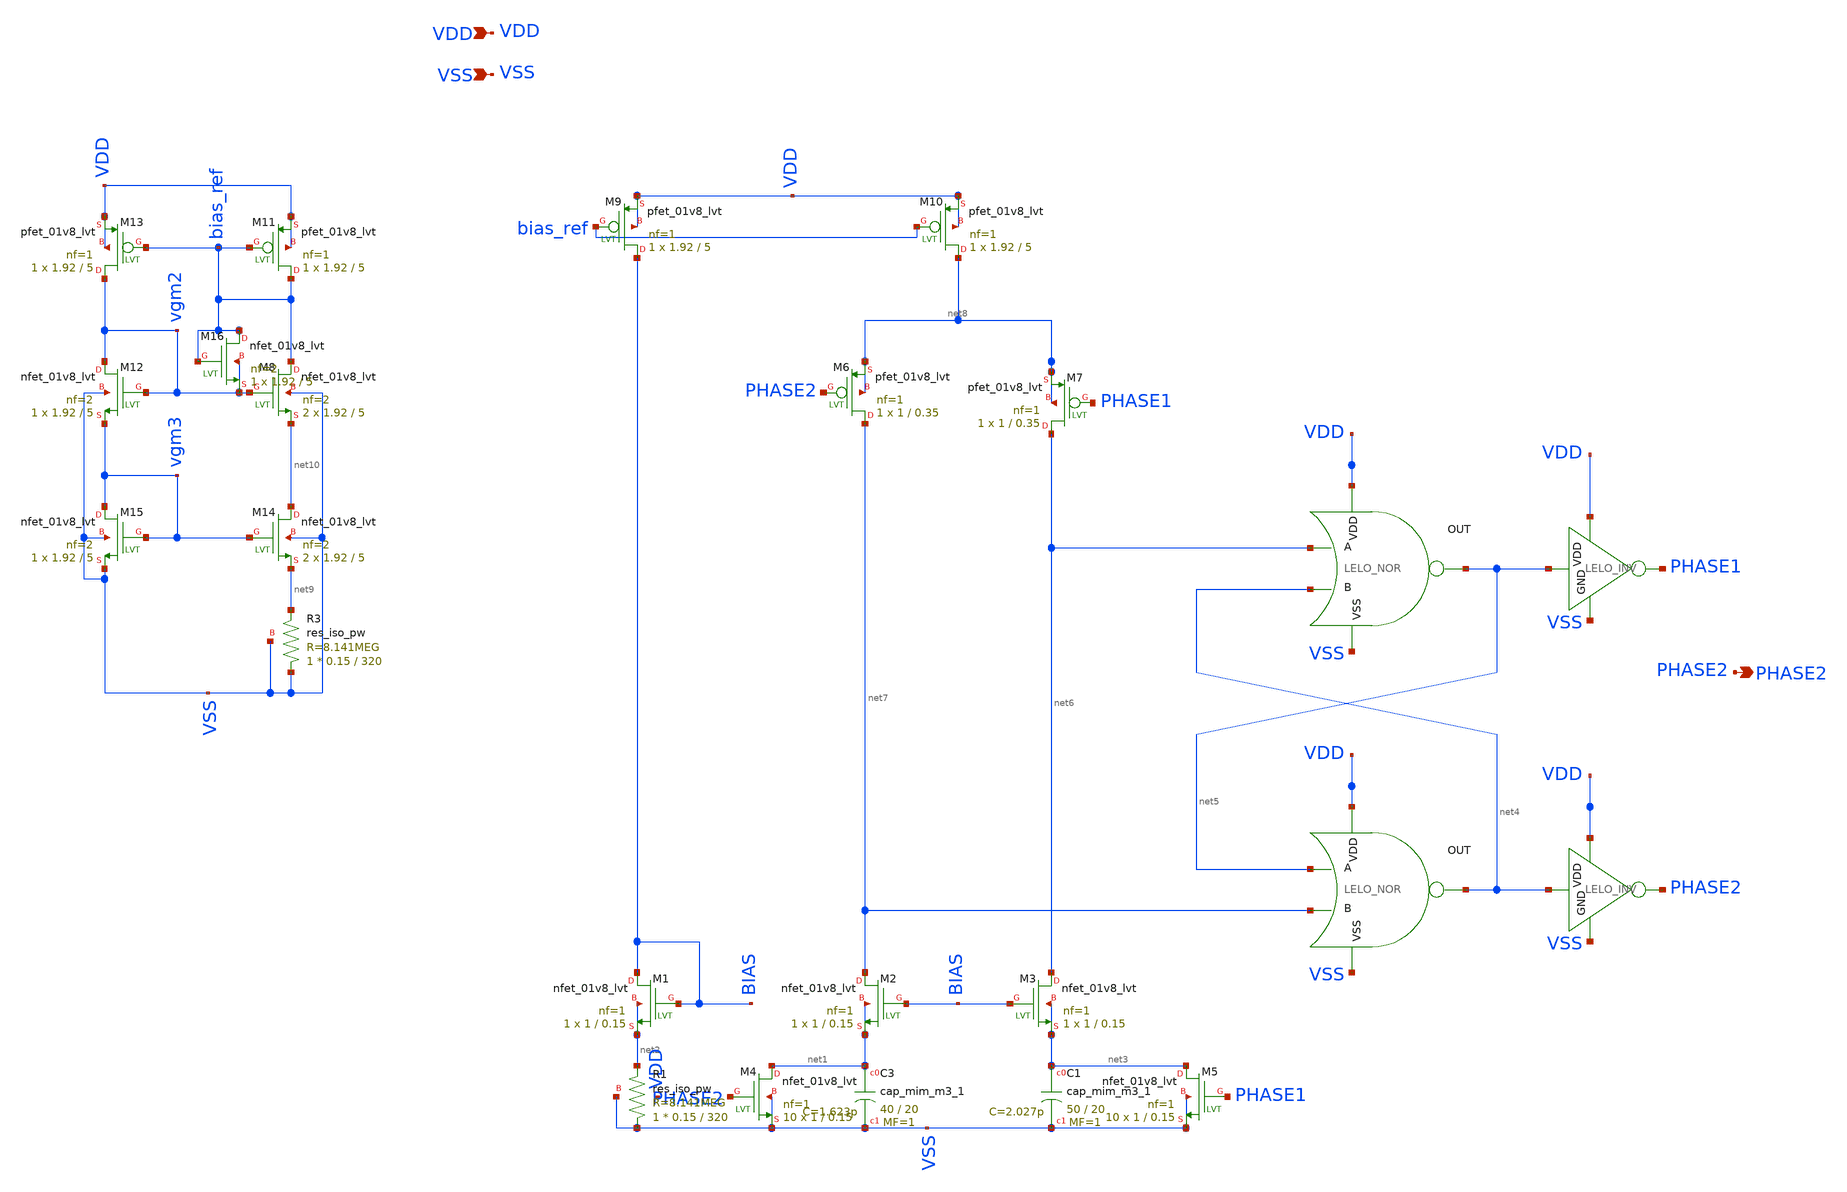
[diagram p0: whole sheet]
** sch_path: design/LELO_SVOD_SKY130A/LELO_SVOD_RELOSC.sch
**.subckt LELO_SVOD_RELOSC VDD VSS PHASE2
*.ipin VDD
*.ipin VSS
*.opin PHASE2
XM1 BIAS BIAS net2 net2 sky130_fd_pr__nfet_01v8_lvt L=0.15 W=1 nf=1 ad='int((1 + 1)/2) * 1 / 1 * 0.29'
+ as='int((1 + 2)/2) * 1 / 1 * 0.29' pd='2*int((1 + 1)/2) * (1 / 1 + 0.29)' ps='2*int((1 + 2)/2) * (1 / 1 + 0.29)'
+ nrd='0.29 / 1 ' nrs='0.29 / 1 ' sa=0 sb=0 sd=0 mult=1 m=1
XM2 net7 BIAS net1 net1 sky130_fd_pr__nfet_01v8_lvt L=0.15 W=1 nf=1 ad='int((1 + 1)/2) * 1 / 1 * 0.29'
+ as='int((1 + 2)/2) * 1 / 1 * 0.29' pd='2*int((1 + 1)/2) * (1 / 1 + 0.29)' ps='2*int((1 + 2)/2) * (1 / 1 + 0.29)'
+ nrd='0.29 / 1 ' nrs='0.29 / 1 ' sa=0 sb=0 sd=0 mult=1 m=1
XM3 net6 BIAS net3 net3 sky130_fd_pr__nfet_01v8_lvt L=0.15 W=1 nf=1 ad='int((1 + 1)/2) * 1 / 1 * 0.29'
+ as='int((1 + 2)/2) * 1 / 1 * 0.29' pd='2*int((1 + 1)/2) * (1 / 1 + 0.29)' ps='2*int((1 + 2)/2) * (1 / 1 + 0.29)'
+ nrd='0.29 / 1 ' nrs='0.29 / 1 ' sa=0 sb=0 sd=0 mult=1 m=1
XM4 net1 PHASE2 VSS VSS sky130_fd_pr__nfet_01v8_lvt L=0.15 W=1 nf=1 ad='int((1 + 1)/2) * 1 / 1 * 0.29'
+ as='int((1 + 2)/2) * 1 / 1 * 0.29' pd='2*int((1 + 1)/2) * (1 / 1 + 0.29)' ps='2*int((1 + 2)/2) * (1 / 1 + 0.29)'
+ nrd='0.29 / 1 ' nrs='0.29 / 1 ' sa=0 sb=0 sd=0 mult=10 m=10
XM5 net3 PHASE1 VSS VSS sky130_fd_pr__nfet_01v8_lvt L=0.15 W=1 nf=1 ad='int((1 + 1)/2) * 1 / 1 * 0.29'
+ as='int((1 + 2)/2) * 1 / 1 * 0.29' pd='2*int((1 + 1)/2) * (1 / 1 + 0.29)' ps='2*int((1 + 2)/2) * (1 / 1 + 0.29)'
+ nrd='0.29 / 1 ' nrs='0.29 / 1 ' sa=0 sb=0 sd=0 mult=10 m=10
x1 VDD net5 net6 net4 VSS LELO_NOR
x2 VDD net4 net5 net7 VSS LELO_NOR
XM6 net7 PHASE2 net8 net8 sky130_fd_pr__pfet_01v8_lvt L=0.35 W=1 nf=1 ad='int((1 + 1)/2) * 1 / 1 * 0.29'
+ as='int((1 + 2)/2) * 1 / 1 * 0.29' pd='2*int((1 + 1)/2) * (1 / 1 + 0.29)' ps='2*int((1 + 2)/2) * (1 / 1 + 0.29)'
+ nrd='0.29 / 1 ' nrs='0.29 / 1 ' sa=0 sb=0 sd=0 mult=1 m=1
XM7 net6 PHASE1 net8 net8 sky130_fd_pr__pfet_01v8_lvt L=0.35 W=1 nf=1 ad='int((1 + 1)/2) * 1 / 1 * 0.29'
+ as='int((1 + 2)/2) * 1 / 1 * 0.29' pd='2*int((1 + 1)/2) * (1 / 1 + 0.29)' ps='2*int((1 + 2)/2) * (1 / 1 + 0.29)'
+ nrd='0.29 / 1 ' nrs='0.29 / 1 ' sa=0 sb=0 sd=0 mult=1 m=1
x3 VDD net5 PHASE1 VSS LELO_INV
x4 VDD net4 PHASE2 VSS LELO_INV
XM9 BIAS bias_ref VDD VDD sky130_fd_pr__pfet_01v8_lvt L=5 W=1.92 nf=1 ad='int((1 + 1)/2) * 1.92 / 1 * 0.29'
+ as='int((1 + 2)/2) * 1.92 / 1 * 0.29' pd='2*int((1 + 1)/2) * (1.92 / 1 + 0.29)' ps='2*int((1 + 2)/2) * (1.92 / 1 + 0.29)'
+ nrd='0.29 / 1.92 ' nrs='0.29 / 1.92 ' sa=0 sb=0 sd=0 mult=1 m=1
XM10 net8 bias_ref VDD VDD sky130_fd_pr__pfet_01v8_lvt L=5 W=1.92 nf=1 ad='int((1 + 1)/2) * 1.92 / 1 * 0.29'
+ as='int((1 + 2)/2) * 1.92 / 1 * 0.29' pd='2*int((1 + 1)/2) * (1.92 / 1 + 0.29)' ps='2*int((1 + 2)/2) * (1.92 / 1 + 0.29)'
+ nrd='0.29 / 1.92 ' nrs='0.29 / 1.92 ' sa=0 sb=0 sd=0 mult=1 m=1
XM8 bias_ref vgm2 net10 VSS sky130_fd_pr__nfet_01v8_lvt L=5 W=1.92 nf=2 ad='int((2 + 1)/2) * 1.92 / 2 * 0.29'
+ as='int((2 + 2)/2) * 1.92 / 2 * 0.29' pd='2*int((2 + 1)/2) * (1.92 / 2 + 0.29)' ps='2*int((2 + 2)/2) * (1.92 / 2 + 0.29)'
+ nrd='0.29 / 1.92 ' nrs='0.29 / 1.92 ' sa=0 sb=0 sd=0 mult=2 m=2
XM11 bias_ref bias_ref VDD VDD sky130_fd_pr__pfet_01v8_lvt L=5 W=1.92 nf=1 ad='int((1 + 1)/2) * 1.92 / 1 * 0.29'
+ as='int((1 + 2)/2) * 1.92 / 1 * 0.29' pd='2*int((1 + 1)/2) * (1.92 / 1 + 0.29)' ps='2*int((1 + 2)/2) * (1.92 / 1 + 0.29)'
+ nrd='0.29 / 1.92 ' nrs='0.29 / 1.92 ' sa=0 sb=0 sd=0 mult=1 m=1
XM12 vgm2 vgm2 vgm3 VSS sky130_fd_pr__nfet_01v8_lvt L=5 W=1.92 nf=2 ad='int((2 + 1)/2) * 1.92 / 2 * 0.29'
+ as='int((2 + 2)/2) * 1.92 / 2 * 0.29' pd='2*int((2 + 1)/2) * (1.92 / 2 + 0.29)' ps='2*int((2 + 2)/2) * (1.92 / 2 + 0.29)'
+ nrd='0.29 / 1.92 ' nrs='0.29 / 1.92 ' sa=0 sb=0 sd=0 mult=1 m=1
XM13 vgm2 bias_ref VDD VDD sky130_fd_pr__pfet_01v8_lvt L=5 W=1.92 nf=1 ad='int((1 + 1)/2) * 1.92 / 1 * 0.29'
+ as='int((1 + 2)/2) * 1.92 / 1 * 0.29' pd='2*int((1 + 1)/2) * (1.92 / 1 + 0.29)' ps='2*int((1 + 2)/2) * (1.92 / 1 + 0.29)'
+ nrd='0.29 / 1.92 ' nrs='0.29 / 1.92 ' sa=0 sb=0 sd=0 mult=1 m=1
XM14 net10 vgm3 net9 VSS sky130_fd_pr__nfet_01v8_lvt L=5 W=1.92 nf=2 ad='int((2 + 1)/2) * 1.92 / 2 * 0.29'
+ as='int((2 + 2)/2) * 1.92 / 2 * 0.29' pd='2*int((2 + 1)/2) * (1.92 / 2 + 0.29)' ps='2*int((2 + 2)/2) * (1.92 / 2 + 0.29)'
+ nrd='0.29 / 1.92 ' nrs='0.29 / 1.92 ' sa=0 sb=0 sd=0 mult=2 m=2
XM15 vgm3 vgm3 VSS VSS sky130_fd_pr__nfet_01v8_lvt L=5 W=1.92 nf=2 ad='int((2 + 1)/2) * 1.92 / 2 * 0.29'
+ as='int((2 + 2)/2) * 1.92 / 2 * 0.29' pd='2*int((2 + 1)/2) * (1.92 / 2 + 0.29)' ps='2*int((2 + 2)/2) * (1.92 / 2 + 0.29)'
+ nrd='0.29 / 1.92 ' nrs='0.29 / 1.92 ' sa=0 sb=0 sd=0 mult=1 m=1
XM16 bias_ref bias_ref vgm2 vgm2 sky130_fd_pr__nfet_01v8_lvt L=5 W=1.92 nf=2 ad='int((2 + 1)/2) * 1.92 / 2 * 0.29'
+ as='int((2 + 2)/2) * 1.92 / 2 * 0.29' pd='2*int((2 + 1)/2) * (1.92 / 2 + 0.29)' ps='2*int((2 + 2)/2) * (1.92 / 2 + 0.29)'
+ nrd='0.29 / 1.92 ' nrs='0.29 / 1.92 ' sa=0 sb=0 sd=0 mult=1 m=1
XC3 net1 VSS sky130_fd_pr__cap_mim_m3_1 W=40 L=20 MF=1 m=1
XC1 net3 VSS sky130_fd_pr__cap_mim_m3_1 W=50 L=20 MF=1 m=1
XR3 VSS net9 VSS sky130_fd_pr__res_iso_pw W=0.15 L=320 m=1
XR1 VSS net2 VSS sky130_fd_pr__res_iso_pw W=0.15 L=320 m=1
**.ends

* expanding   symbol:  LELO_SVOD_SKY130A/LELO_NOR.sym # of pins=5
** sym_path: design/LELO_SVOD_SKY130A/LELO_NOR.sym
** sch_path: design/LELO_SVOD_SKY130A/LELO_NOR.sch
.subckt LELO_NOR VDD OUT A B VSS
*.ipin VDD
*.ipin VSS
*.opin OUT
*.ipin A
*.ipin B
XM2 OUT B VSS VSS sky130_fd_pr__nfet_01v8 L=0.15 W=2 nf=1 ad='int((1 + 1)/2) * 2 / 1 * 0.29' as='int((1 + 2)/2) * 2 / 1 * 0.29'
+ pd='2*int((1 + 1)/2) * (2 / 1 + 0.29)' ps='2*int((1 + 2)/2) * (2 / 1 + 0.29)' nrd='0.29 / 2 ' nrs='0.29 / 2 '
+ sa=0 sb=0 sd=0 mult=1 m=1
XM1 OUT A VSS VSS sky130_fd_pr__nfet_01v8 L=0.15 W=2 nf=1 ad='int((1 + 1)/2) * 2 / 1 * 0.29' as='int((1 + 2)/2) * 2 / 1 * 0.29'
+ pd='2*int((1 + 1)/2) * (2 / 1 + 0.29)' ps='2*int((1 + 2)/2) * (2 / 1 + 0.29)' nrd='0.29 / 2 ' nrs='0.29 / 2 '
+ sa=0 sb=0 sd=0 mult=1 m=1
XM3 OUT B net1 VDD sky130_fd_pr__pfet_01v8 L=0.15 W=4 nf=1 ad='int((1 + 1)/2) * 4 / 1 * 0.29' as='int((1 + 2)/2) * 4 / 1 * 0.29'
+ pd='2*int((1 + 1)/2) * (4 / 1 + 0.29)' ps='2*int((1 + 2)/2) * (4 / 1 + 0.29)' nrd='0.29 / 4 ' nrs='0.29 / 4 '
+ sa=0 sb=0 sd=0 mult=1 m=1
XM4 net1 A VDD VDD sky130_fd_pr__pfet_01v8 L=0.15 W=4 nf=1 ad='int((1 + 1)/2) * 4 / 1 * 0.29' as='int((1 + 2)/2) * 4 / 1 * 0.29'
+ pd='2*int((1 + 1)/2) * (4 / 1 + 0.29)' ps='2*int((1 + 2)/2) * (4 / 1 + 0.29)' nrd='0.29 / 4 ' nrs='0.29 / 4 '
+ sa=0 sb=0 sd=0 mult=1 m=1
.ends


* expanding   symbol:  LELO_SVOD_SKY130A/LELO_INV.sym # of pins=4
** sym_path: design/LELO_SVOD_SKY130A/LELO_INV.sym
** sch_path: design/LELO_SVOD_SKY130A/LELO_INV.sch
.subckt LELO_INV VDD VIN VOUT GND
*.ipin VIN
*.ipin VDD
*.ipin GND
*.opin VOUT
XM1 VOUT VIN GND GND sky130_fd_pr__nfet_01v8_lvt L=0.15 W=1 nf=1 ad='int((1 + 1)/2) * 1 / 1 * 0.29' as='int((1 + 2)/2) * 1 / 1 * 0.29'
+ pd='2*int((1 + 1)/2) * (1 / 1 + 0.29)' ps='2*int((1 + 2)/2) * (1 / 1 + 0.29)' nrd='0.29 / 1 ' nrs='0.29 / 1 '
+ sa=0 sb=0 sd=0 mult=1 m=1
XM2 VOUT VIN VDD VDD sky130_fd_pr__pfet_01v8_lvt L=0.35 W=1 nf=1 ad='int((1 + 1)/2) * 1 / 1 * 0.29' as='int((1 + 2)/2) * 1 / 1 * 0.29'
+ pd='2*int((1 + 1)/2) * (1 / 1 + 0.29)' ps='2*int((1 + 2)/2) * (1 / 1 + 0.29)' nrd='0.29 / 1 ' nrs='0.29 / 1 '
+ sa=0 sb=0 sd=0 mult=2 m=2
.ends

.end
